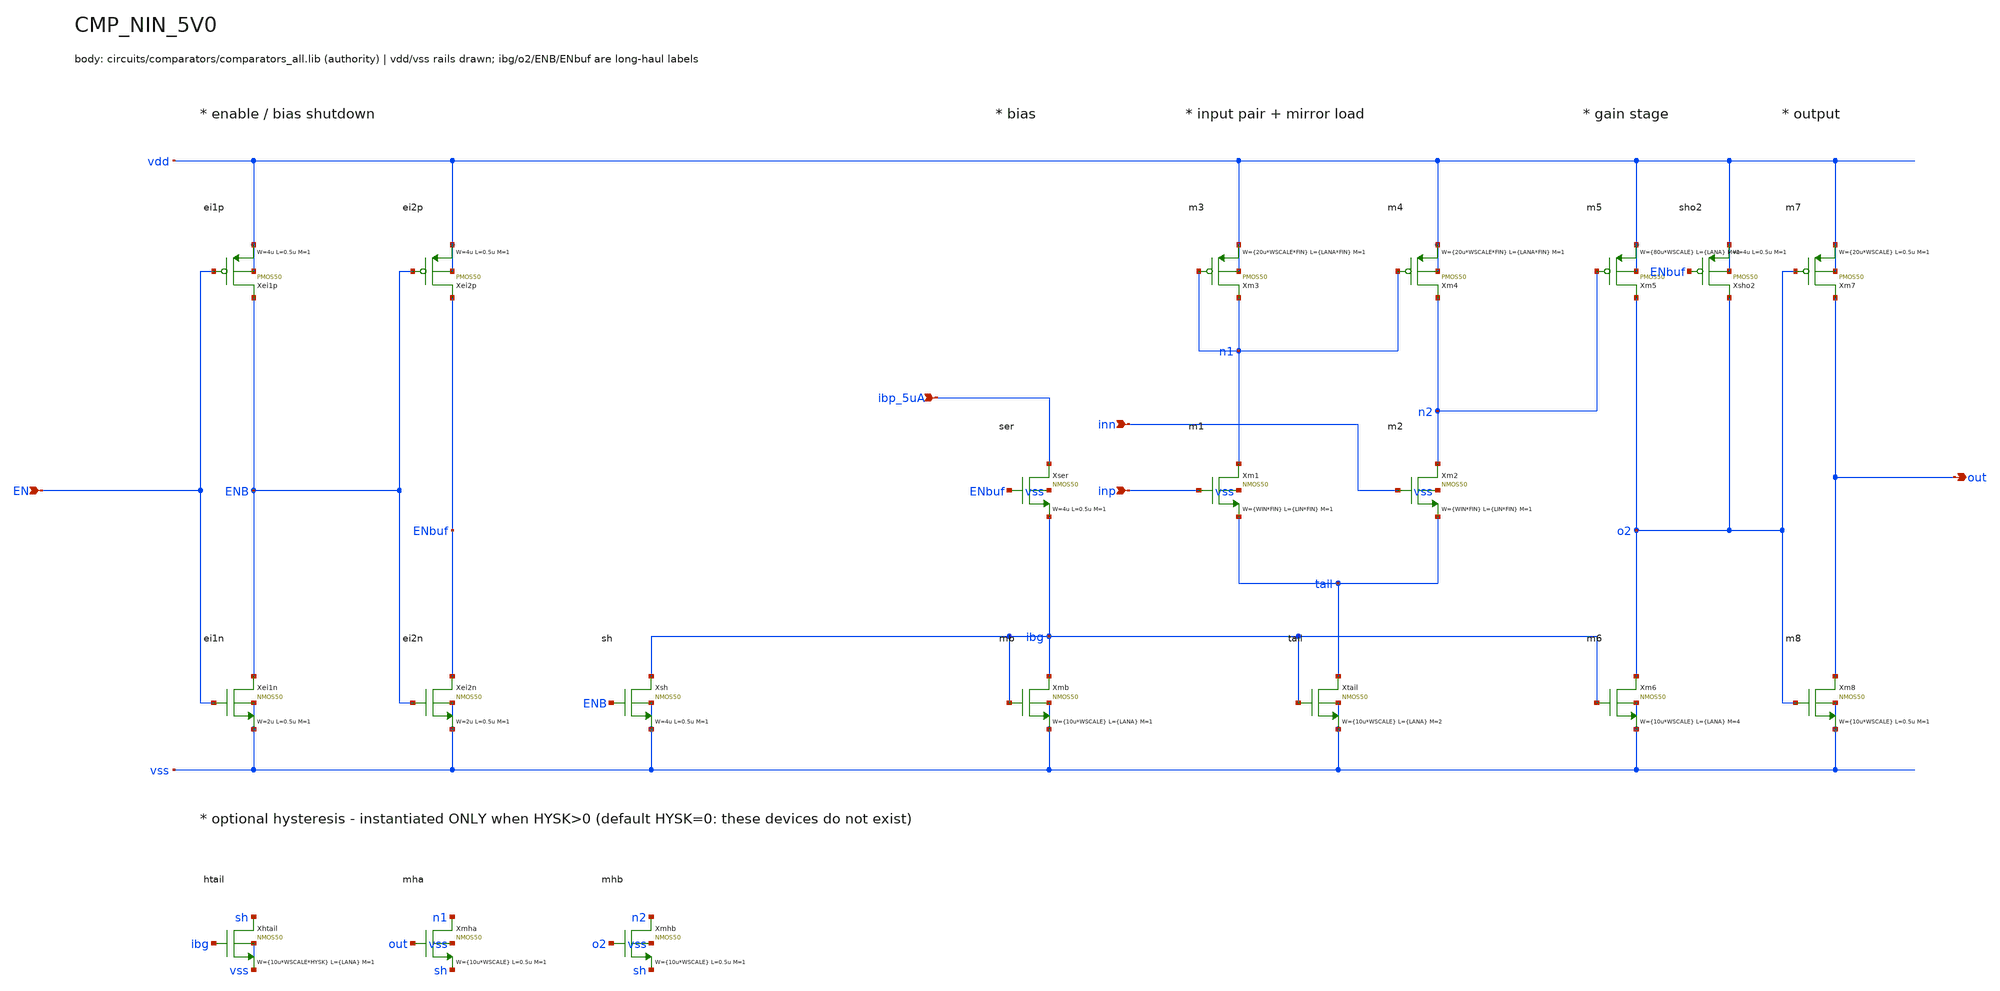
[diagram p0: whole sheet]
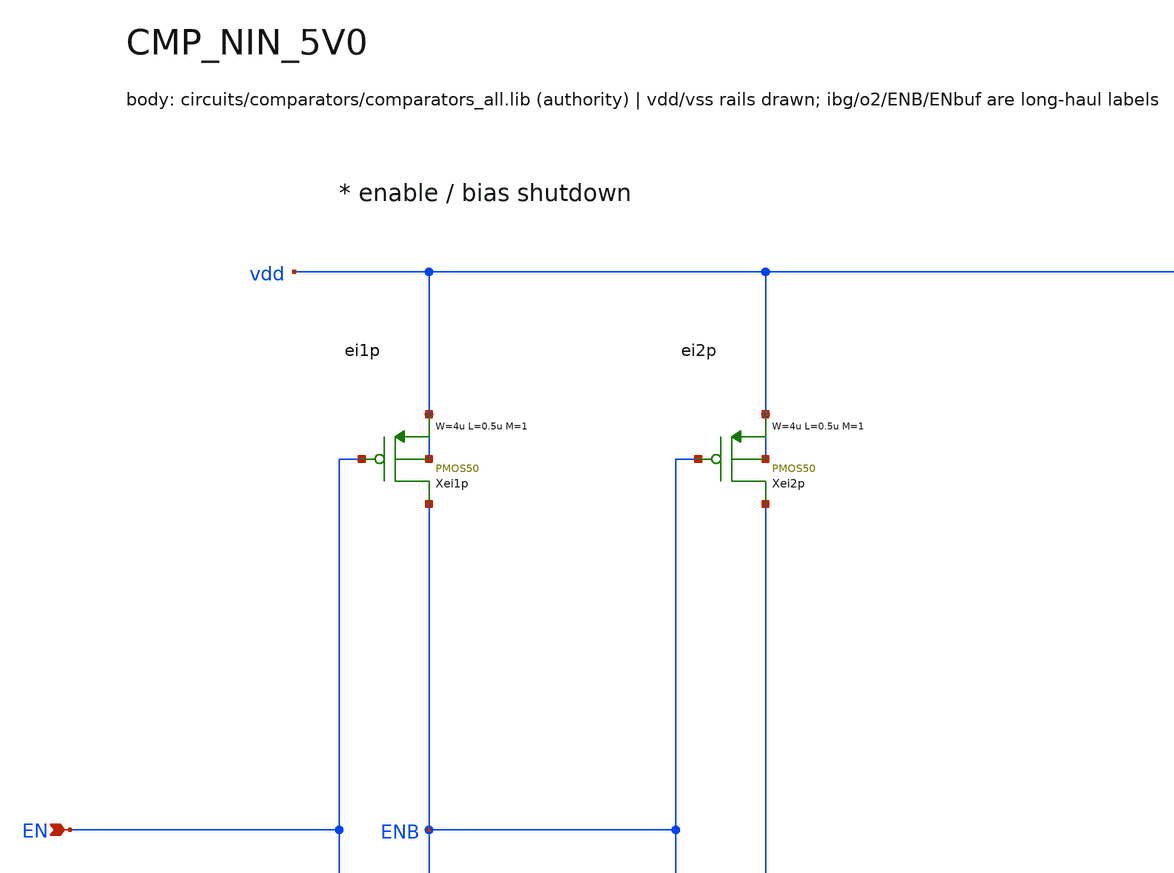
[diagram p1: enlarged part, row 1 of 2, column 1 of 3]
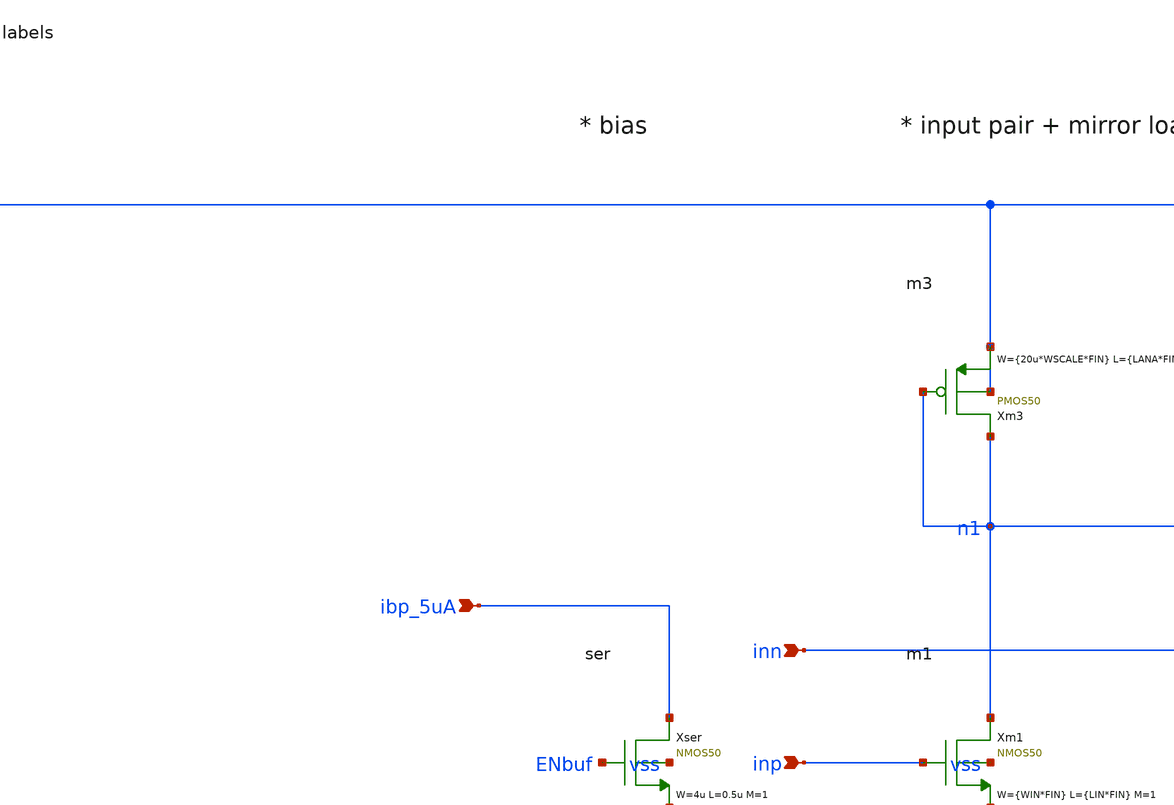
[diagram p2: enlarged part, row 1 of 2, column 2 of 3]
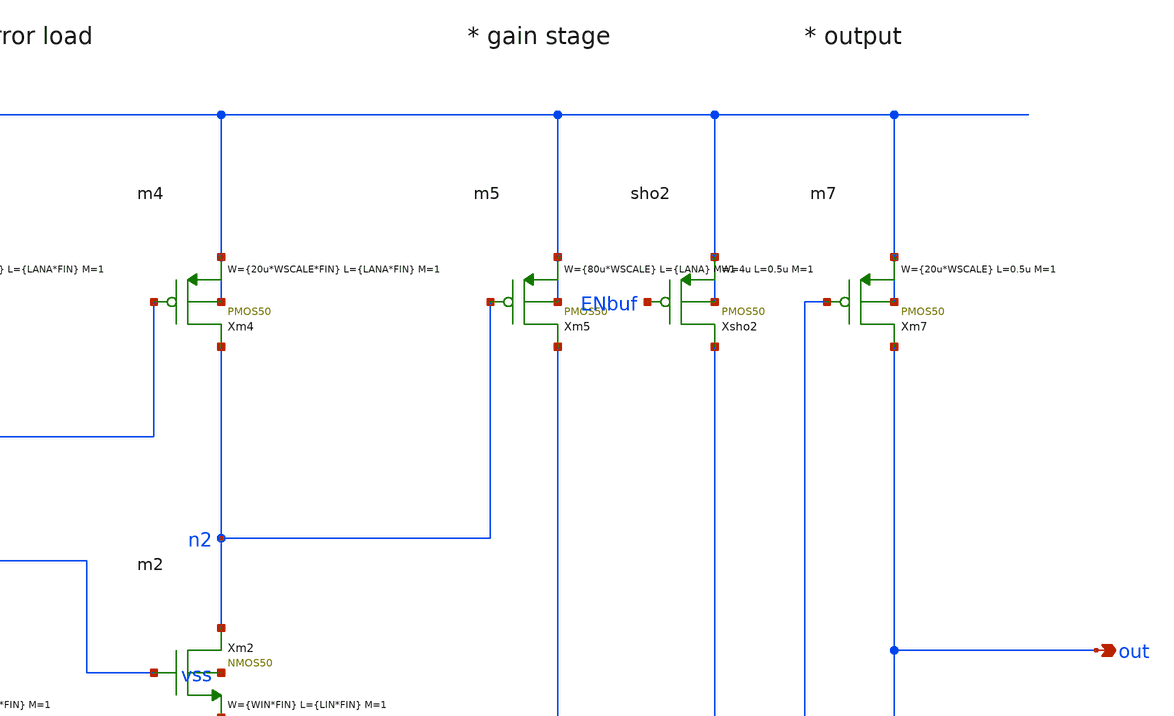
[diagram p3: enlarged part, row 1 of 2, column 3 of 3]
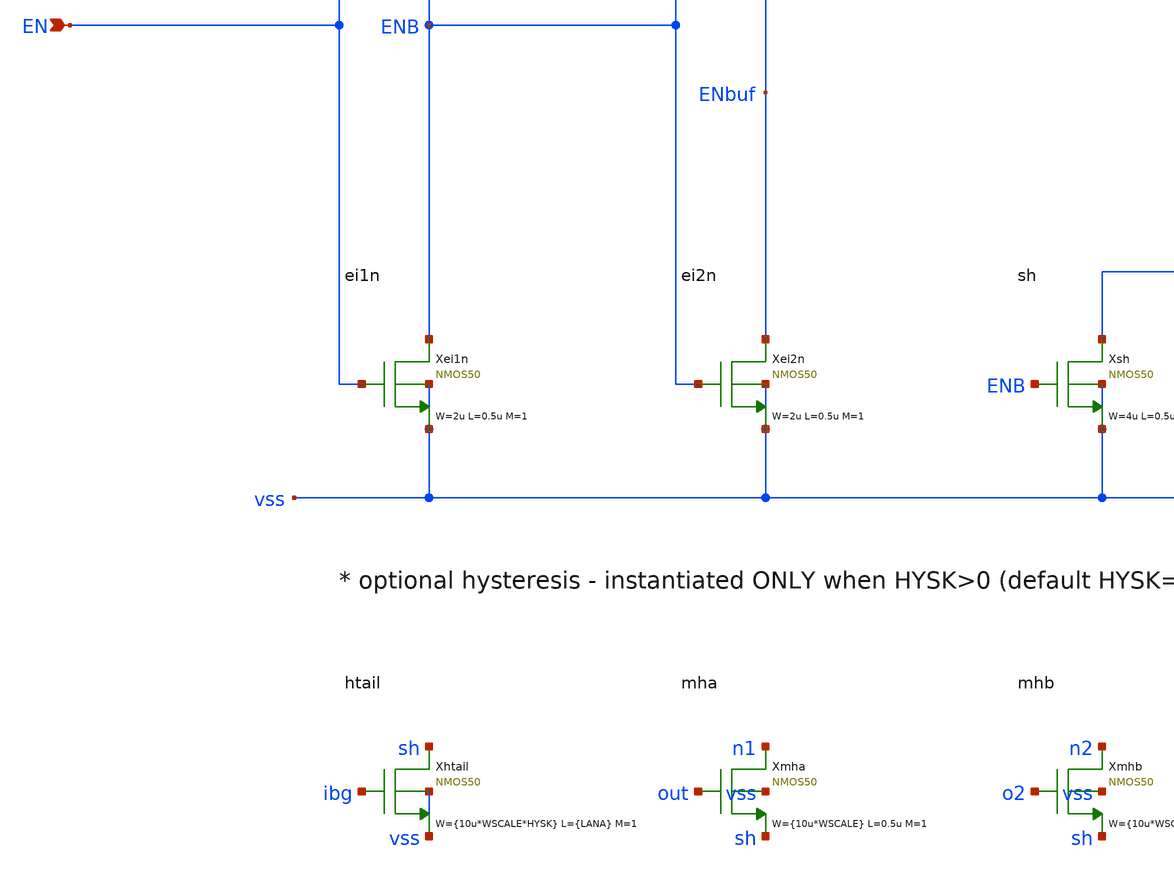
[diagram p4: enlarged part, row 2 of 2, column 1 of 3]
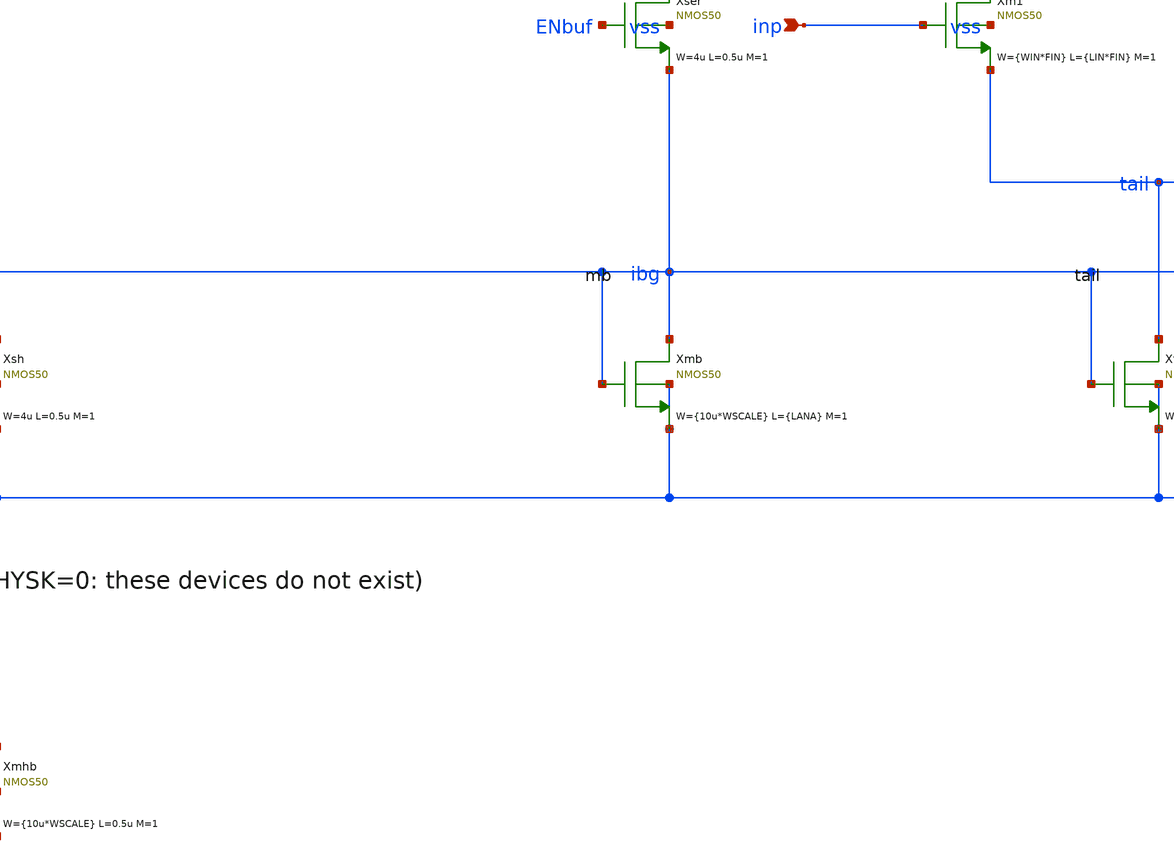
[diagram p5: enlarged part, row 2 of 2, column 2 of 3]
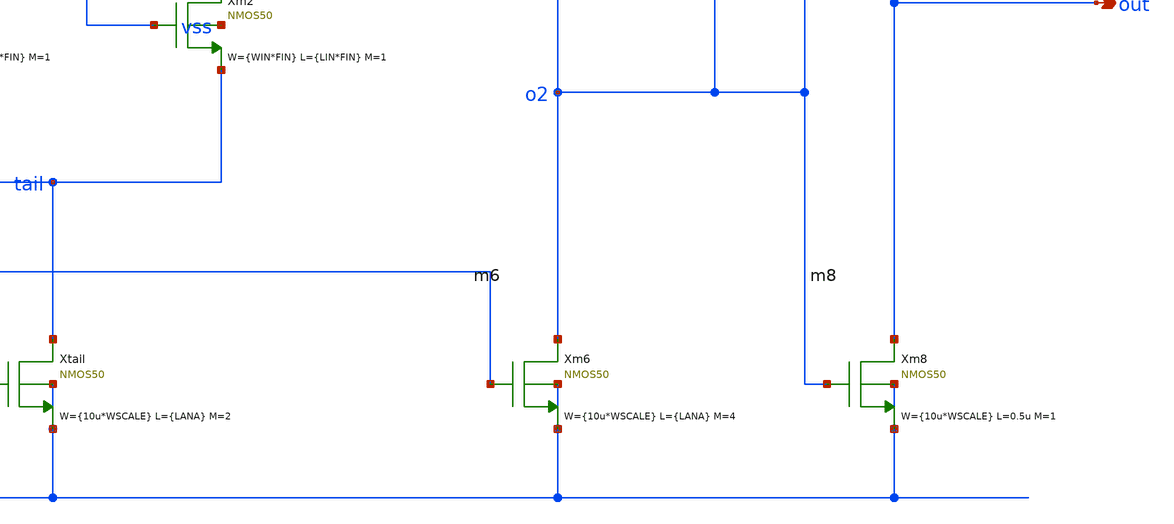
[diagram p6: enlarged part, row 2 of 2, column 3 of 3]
** sch_path: xschem/comparators/CMP_NIN_5V0.sch
**.subckt CMP_NIN_5V0 ibp_5uA out inp inn EN
*.ipin ibp_5uA
*.opin out
*.ipin inp
*.ipin inn
*.ipin EN
Xmb ibg ibg vss vss NMOS50 W={10u*WSCALE} L={LANA} M=1 MM_SIGMA=0
Xtail tail ibg vss vss NMOS50 W={10u*WSCALE} L={LANA} M=2 MM_SIGMA=0
Xm1 n1 inp tail vss NMOS50 W={WIN*FIN} L={LIN*FIN} M=1 MM_SIGMA=0
Xm2 n2 inn tail vss NMOS50 W={WIN*FIN} L={LIN*FIN} M=1 MM_SIGMA=0
Xm3 n1 n1 vdd vdd PMOS50 W={20u*WSCALE*FIN} L={LANA*FIN} M=1 MM_SIGMA=0
Xm4 n2 n1 vdd vdd PMOS50 W={20u*WSCALE*FIN} L={LANA*FIN} M=1 MM_SIGMA=0
Xm5 o2 n2 vdd vdd PMOS50 W={80u*WSCALE} L={LANA} M=1 MM_SIGMA=0
Xm6 o2 ibg vss vss NMOS50 W={10u*WSCALE} L={LANA} M=4 MM_SIGMA=0
Xm7 out o2 vdd vdd PMOS50 W={20u*WSCALE} L=0.5u M=1 MM_SIGMA=0
Xm8 out o2 vss vss NMOS50 W={10u*WSCALE} L=0.5u M=1 MM_SIGMA=0
Xei1p ENB EN vdd vdd PMOS50 W=4u L=0.5u M=1 MM_SIGMA=0
Xei1n ENB EN vss vss NMOS50 W=2u L=0.5u M=1 MM_SIGMA=0
Xei2p ENbuf ENB vdd vdd PMOS50 W=4u L=0.5u M=1 MM_SIGMA=0
Xei2n ENbuf ENB vss vss NMOS50 W=2u L=0.5u M=1 MM_SIGMA=0
Xsh ibg ENB vss vss NMOS50 W=4u L=0.5u M=1 MM_SIGMA=0
Xsho2 o2 ENbuf vdd vdd PMOS50 W=4u L=0.5u M=1 MM_SIGMA=0
Xser ibp_5uA ENbuf ibg vss NMOS50 W=4u L=0.5u M=1 MM_SIGMA=0
Xhtail sh ibg vss vss NMOS50 W={10u*WSCALE*HYSK} L={LANA} M=1 MM_SIGMA=0
Xmha n1 out sh vss NMOS50 W={10u*WSCALE} L=0.5u M=1 MM_SIGMA=0
Xmhb n2 o2 sh vss NMOS50 W={10u*WSCALE} L=0.5u M=1 MM_SIGMA=0
**.ends
.end
